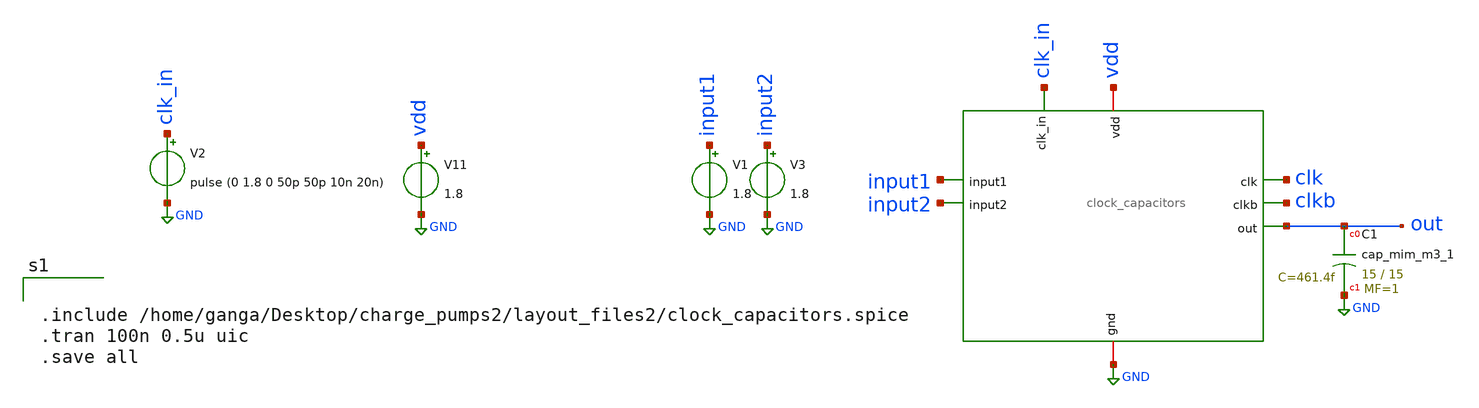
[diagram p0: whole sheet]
** sch_path: xschem/test_clock_cap.sch
**.subckt test_clock_cap
x1 out clk clkb clk_in input1 input2 vdd GND clock_capacitors
V2 clk_in GND pulse (0 1.8 0 50p 50p 10n 20n)
V11 vdd GND 1.8
V1 input1 GND 1.8
V3 input2 GND 1.8
XC1 out GND sky130_fd_pr__cap_mim_m3_1 W=15 L=15 MF=1 m=1
**** begin user architecture code

** opencircuitdesign pdks install
.lib $::SKYWATER_MODELS/sky130.lib.spice tt




.include /home/ganga/Desktop/charge_pumps2/layout_files2/clock_capacitors.spice
.tran 100n 0.5u uic
.save all


**** end user architecture code
**.ends
.GLOBAL GND
.end
